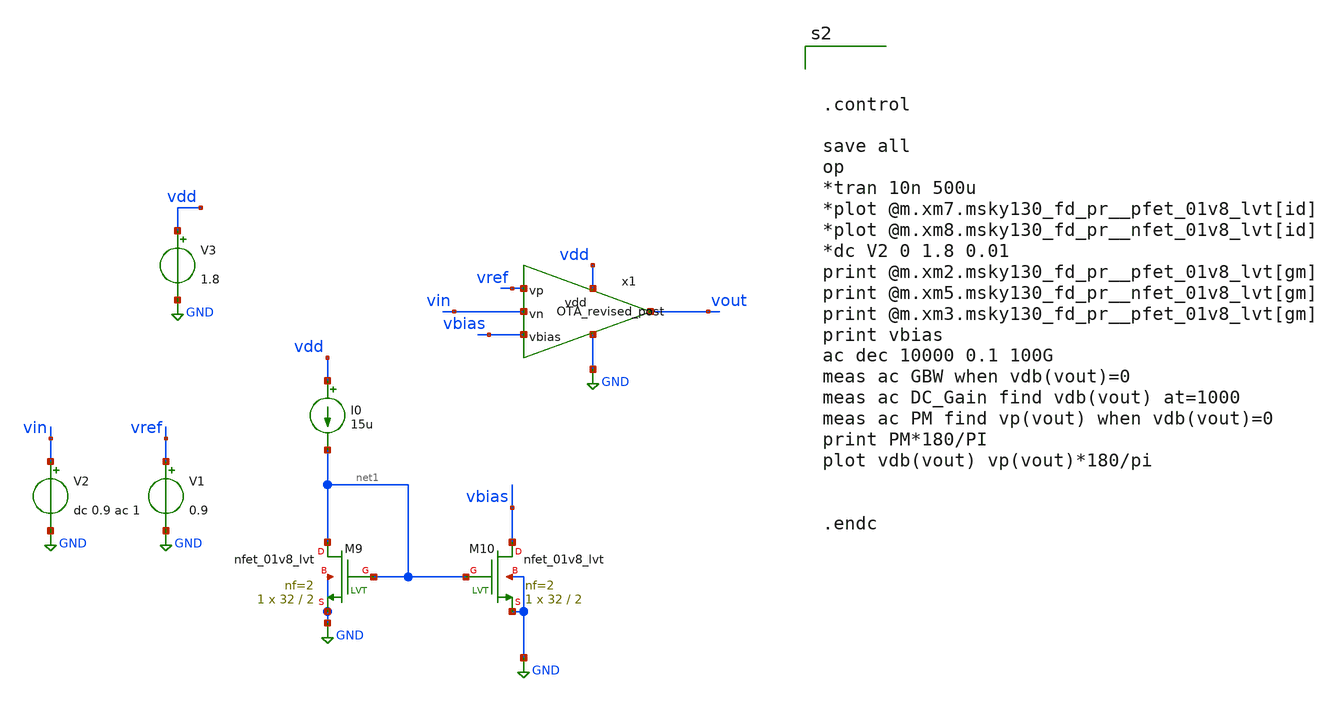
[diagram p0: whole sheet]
** sch_path: xschem/src/OTA/OTA_tb2.sch
**.subckt OTA_tb2
V3 vdd GND 1.8
V2 vin GND dc 0.9 ac 1
V1 vref GND 0.9
I0 vdd net1 15u
XM9 net1 net1 GND GND sky130_fd_pr__nfet_01v8_lvt L=2 W=32 nf=2 ad='int((nf+1)/2) * W/nf * 0.29' as='int((nf+2)/2) * W/nf * 0.29'
+ pd='2*int((nf+1)/2) * (W/nf + 0.29)' ps='2*int((nf+2)/2) * (W/nf + 0.29)' nrd='0.29 / W' nrs='0.29 / W'
+ sa=0 sb=0 sd=0 mult=1 m=1
XM10 vbias net1 GND GND sky130_fd_pr__nfet_01v8_lvt L=2 W=32 nf=2 ad='int((nf+1)/2) * W/nf * 0.29' as='int((nf+2)/2) * W/nf * 0.29'
+ pd='2*int((nf+1)/2) * (W/nf + 0.29)' ps='2*int((nf+2)/2) * (W/nf + 0.29)' nrd='0.29 / W' nrs='0.29 / W'
+ sa=0 sb=0 sd=0 mult=1 m=1
x1 vdd vref vin vbias GND vout OTA_revised_post
**** begin user architecture code

.include /home/eda/pdk/skywater-pdk/libraries/sky130_fd_pr_ngspice/latest/models/corners/ss.spice
.include /home/eda/magic/class_d_audio_amplifier/OTA/OTA_post.spice
.include /home/eda/magic/class_d_audio_amplifier/OTA/OTA_revised_post.spice
.include /home/eda/magic/class_d_audio_amplifier/OTA/OTA_tri_post.spice
.include /home/eda/magic/class_d_audio_amplifier/OTA/OTA_int_post.spice
* Resistor$::SKYWATER_MODELS/Capacitor
.include $::SKYWATER_MODELS/models/r+c/res_typical__cap_typical.spice
.include $::SKYWATER_MODELS/models/r+c/res_typical__cap_typical__lin.spice
* Special cells
.include $::SKYWATER_MODELS/models/corners/tt/specialized_cells.spice





.control

save all
op
*tran 10n 500u
*plot @m.xm7.msky130_fd_pr__pfet_01v8_lvt[id]
*plot @m.xm8.msky130_fd_pr__nfet_01v8_lvt[id]
*dc V2 0 1.8 0.01
print @m.xm2.msky130_fd_pr__pfet_01v8_lvt[gm]
print @m.xm5.msky130_fd_pr__nfet_01v8_lvt[gm]
print @m.xm3.msky130_fd_pr__pfet_01v8_lvt[gm]
print vbias
ac dec 10000 0.1 100G
meas ac GBW when vdb(vout)=0
meas ac DC_Gain find vdb(vout) at=1000
meas ac PM find vp(vout) when vdb(vout)=0
print PM*180/PI
plot vdb(vout) vp(vout)*180/pi


.endc


**** end user architecture code
**.ends
.GLOBAL GND
.end
